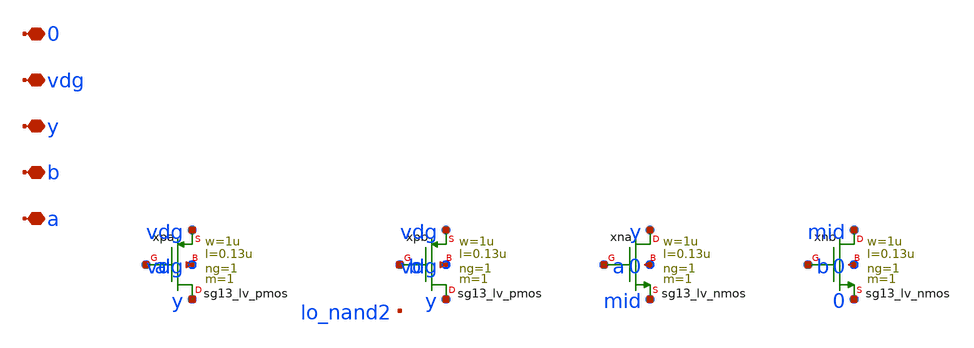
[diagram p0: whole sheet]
** sch_path: analog/lo/sch/lo_nand2.sch
**.subckt lo_nand2 a b y vdg 0
*.iopin a
*.iopin b
*.iopin y
*.iopin vdg
*.iopin 0
Xxpa y a vdg vdg sg13_lv_pmos w=1u l=0.13u ng=1 m=1 mm_ok=1
Xxpb y b vdg vdg sg13_lv_pmos w=1u l=0.13u ng=1 m=1 mm_ok=1
Xxna y a mid 0 sg13_lv_nmos w=1u l=0.13u ng=1 m=1 mm_ok=1
Xxnb mid b 0 0 sg13_lv_nmos w=1u l=0.13u ng=1 m=1 mm_ok=1
**.ends
.end
